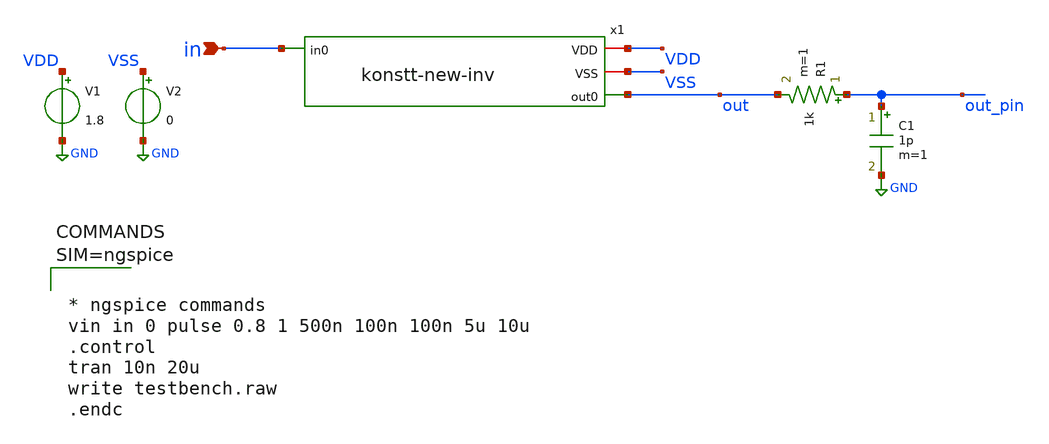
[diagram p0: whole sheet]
** sch_path: xschem/testbench.sch
**.subckt testbench in
*.ipin in
x1 VDD VSS out in konstt-new-inv
V1 VDD GND 1.8
V2 VSS GND 0
R1 out_pin out 1k m=1
C1 out_pin GND 1p m=1
**** begin user architecture code

** opencircuitdesign pdks install
.lib $::SKYWATER_MODELS/sky130.lib.spice tt





* ngspice commands
vin in 0 pulse 0.8 1 500n 100n 100n 5u 10u
.control
tran 10n 20u
write testbench.raw
.endc




**** end user architecture code
**.ends

* expanding   symbol:  konstt-new-inv.sym # of pins=4
** sym_path: xschem/konstt-new-inv.sym
** sch_path: xschem/konstt-new-inv.sch
.subckt konstt-new-inv VDD VSS out0 in0
*.iopin VDD
*.iopin VSS
*.ipin in0
*.opin out0
XM1 inverted in0 VDD VDD sky130_fd_pr__pfet_01v8 L=0.15 W=1 nf=1 ad='int((nf+1)/2) * W/nf * 0.29' as='int((nf+2)/2) * W/nf * 0.29'
+ pd='2*int((nf+1)/2) * (W/nf + 0.29)' ps='2*int((nf+2)/2) * (W/nf + 0.29)' nrd='0.29 / W' nrs='0.29 / W'
+ sa=0 sb=0 sd=0 mult=1 m=1
XM2 inverted in0 VSS VSS sky130_fd_pr__nfet_01v8 L=0.15 W=1 nf=1 ad='int((nf+1)/2) * W/nf * 0.29' as='int((nf+2)/2) * W/nf * 0.29'
+ pd='2*int((nf+1)/2) * (W/nf + 0.29)' ps='2*int((nf+2)/2) * (W/nf + 0.29)' nrd='0.29 / W' nrs='0.29 / W'
+ sa=0 sb=0 sd=0 mult=1 m=1
XM3 out0 inverted VDD VDD sky130_fd_pr__pfet_01v8 L=0.15 W=20 nf=20 ad='int((nf+1)/2) * W/nf * 0.29'
+ as='int((nf+2)/2) * W/nf * 0.29' pd='2*int((nf+1)/2) * (W/nf + 0.29)' ps='2*int((nf+2)/2) * (W/nf + 0.29)'
+ nrd='0.29 / W' nrs='0.29 / W' sa=0 sb=0 sd=0 mult=1 m=1
XM4 out0 inverted VSS VSS sky130_fd_pr__nfet_01v8 L=0.15 W=20 nf=20 ad='int((nf+1)/2) * W/nf * 0.29'
+ as='int((nf+2)/2) * W/nf * 0.29' pd='2*int((nf+1)/2) * (W/nf + 0.29)' ps='2*int((nf+2)/2) * (W/nf + 0.29)'
+ nrd='0.29 / W' nrs='0.29 / W' sa=0 sb=0 sd=0 mult=1 m=1
.ends

.GLOBAL GND
.end
